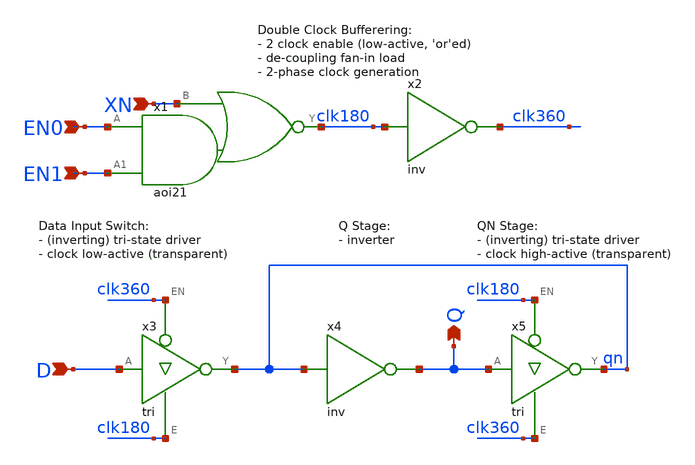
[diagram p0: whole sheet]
** sch_path: Sources/crafted/LATEEN.sch
**.subckt LATEEN XN D Q EN0 EN1
*.ipin XN
*.ipin D
*.opin Q
*.ipin EN0
*.ipin EN1
x2 clk180 clk360 VDD GND inv Wmin=1.5u Lmin=1u g=2 m=1
x4 qn Q VDD GND inv Wmin=1.5u Lmin=1u g=2 m=1
x3 D clk360 clk180 qn VDD GND tri Wmin=1.5u Lmin=1u g=2 m=1
x5 Q clk180 clk360 qn VDD GND tri Wmin=1.5u Lmin=1u g=2 m=1
x1 EN0 EN1 clk180 XN VDD GND aoi21 Wmin=1.5u Lmin=1u g=2 m=1
**.ends
.end
